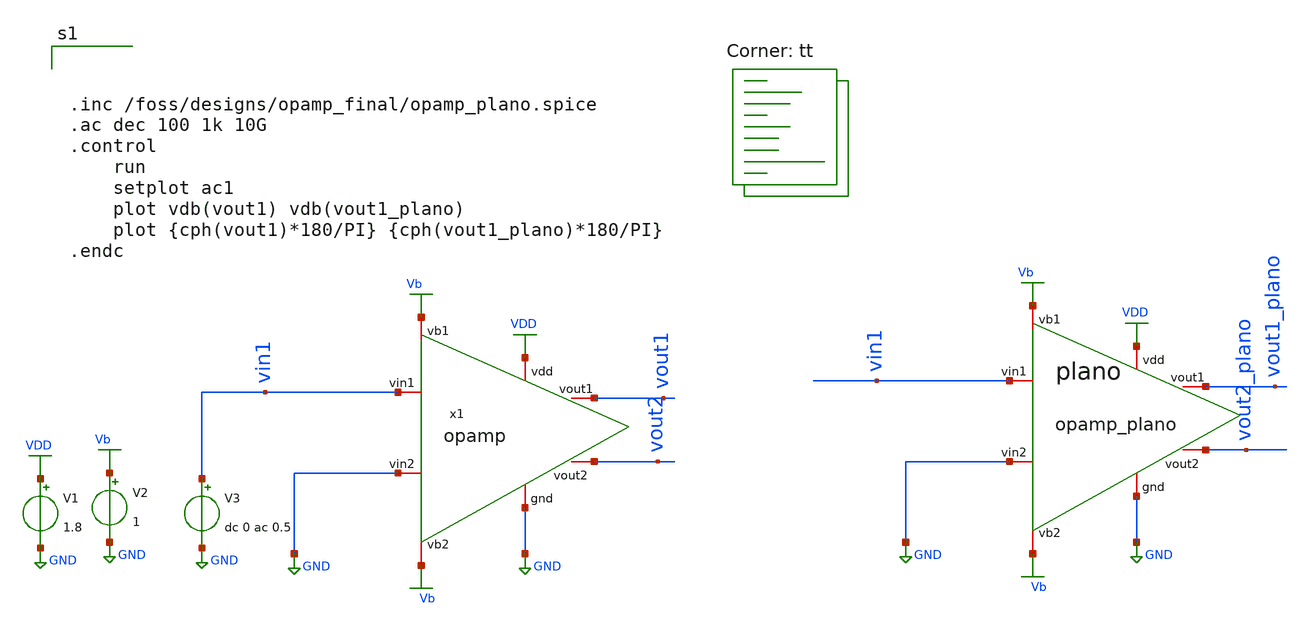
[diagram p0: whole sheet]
** sch_path: DIA3/opamp_final/tb_opamp_con_pex.sch
**.subckt tb_opamp_con_pex
x1 VDD Vb GND vin1 vout2 vout1 Vb GND opamp
V1 VDD GND 1.8
V3 vin1 GND dc 0 ac 0.5
V2 Vb GND 1
x1 VDD Vb GND vin1 vout2_plano vout1_plano GND Vb opamp_plano
**** begin user architecture code
.lib $::SKYWATER_MODELS/sky130.lib.spice tt



.inc /foss/designs/opamp_final/opamp_plano.spice
.ac dec 100 1k 10G
.control
	run
	setplot ac1
	plot vdb(vout1) vdb(vout1_plano)
	plot {cph(vout1)*180/PI} {cph(vout1_plano)*180/PI}
.endc



**** end user architecture code
**.ends

* expanding   symbol:  opamp.sym # of pins=8
** sym_path: DIA3/opamp_final/opamp.sym
** sch_path: DIA3/opamp_final/opamp.sch
.subckt opamp vdd vb1 vin2 vin1 vout2 vout1 vb2 gnd
*.iopin vdd
*.iopin gnd
*.iopin vout1
*.iopin vout2
*.iopin vin1
*.iopin vin2
*.iopin vb1
*.iopin vb2
XM1 X vb1 vdd vdd sky130_fd_pr__pfet_01v8 L=0.15 W=2.27 nf=1 ad='int((nf+1)/2) * W/nf * 0.29' as='int((nf+2)/2) * W/nf * 0.29'
+ pd='2*int((nf+1)/2) * (W/nf + 0.29)' ps='2*int((nf+2)/2) * (W/nf + 0.29)' nrd='0.29 / W' nrs='0.29 / W'
+ sa=0 sb=0 sd=0 mult=1 m=1
XM2 Y vb1 vdd vdd sky130_fd_pr__pfet_01v8 L=0.15 W=2.27 nf=1 ad='int((nf+1)/2) * W/nf * 0.29' as='int((nf+2)/2) * W/nf * 0.29'
+ pd='2*int((nf+1)/2) * (W/nf + 0.29)' ps='2*int((nf+2)/2) * (W/nf + 0.29)' nrd='0.29 / W' nrs='0.29 / W'
+ sa=0 sb=0 sd=0 mult=1 m=1
XM3 X vin2 net1 gnd sky130_fd_pr__nfet_01v8 L=0.15 W=0.86 nf=1 ad='int((nf+1)/2) * W/nf * 0.29' as='int((nf+2)/2) * W/nf * 0.29'
+ pd='2*int((nf+1)/2) * (W/nf + 0.29)' ps='2*int((nf+2)/2) * (W/nf + 0.29)' nrd='0.29 / W' nrs='0.29 / W'
+ sa=0 sb=0 sd=0 mult=1 m=1
XM4 Y vin1 net1 gnd sky130_fd_pr__nfet_01v8 L=0.15 W=0.86 nf=1 ad='int((nf+1)/2) * W/nf * 0.29' as='int((nf+2)/2) * W/nf * 0.29'
+ pd='2*int((nf+1)/2) * (W/nf + 0.29)' ps='2*int((nf+2)/2) * (W/nf + 0.29)' nrd='0.29 / W' nrs='0.29 / W'
+ sa=0 sb=0 sd=0 mult=1 m=1
XM5 net1 net2 gnd gnd sky130_fd_pr__nfet_01v8 L=0.15 W=0.49 nf=1 ad='int((nf+1)/2) * W/nf * 0.29' as='int((nf+2)/2) * W/nf * 0.29'
+ pd='2*int((nf+1)/2) * (W/nf + 0.29)' ps='2*int((nf+2)/2) * (W/nf + 0.29)' nrd='0.29 / W' nrs='0.29 / W'
+ sa=0 sb=0 sd=0 mult=1 m=1
XM6 vout1 Y vdd vdd sky130_fd_pr__pfet_01v8 L=0.15 W=56.9 nf=1 ad='int((nf+1)/2) * W/nf * 0.29' as='int((nf+2)/2) * W/nf * 0.29'
+ pd='2*int((nf+1)/2) * (W/nf + 0.29)' ps='2*int((nf+2)/2) * (W/nf + 0.29)' nrd='0.29 / W' nrs='0.29 / W'
+ sa=0 sb=0 sd=0 mult=1 m=1
XM7 vout2 X vdd vdd sky130_fd_pr__pfet_01v8 L=0.15 W=56.9 nf=1 ad='int((nf+1)/2) * W/nf * 0.29' as='int((nf+2)/2) * W/nf * 0.29'
+ pd='2*int((nf+1)/2) * (W/nf + 0.29)' ps='2*int((nf+2)/2) * (W/nf + 0.29)' nrd='0.29 / W' nrs='0.29 / W'
+ sa=0 sb=0 sd=0 mult=1 m=1
XM8 vout1 vb2 gnd gnd sky130_fd_pr__nfet_01v8 L=0.15 W=1.34 nf=1 ad='int((nf+1)/2) * W/nf * 0.29' as='int((nf+2)/2) * W/nf * 0.29'
+ pd='2*int((nf+1)/2) * (W/nf + 0.29)' ps='2*int((nf+2)/2) * (W/nf + 0.29)' nrd='0.29 / W' nrs='0.29 / W'
+ sa=0 sb=0 sd=0 mult=1 m=1
XM9 vout2 vb2 gnd gnd sky130_fd_pr__nfet_01v8 L=0.15 W=1.34 nf=1 ad='int((nf+1)/2) * W/nf * 0.29' as='int((nf+2)/2) * W/nf * 0.29'
+ pd='2*int((nf+1)/2) * (W/nf + 0.29)' ps='2*int((nf+2)/2) * (W/nf + 0.29)' nrd='0.29 / W' nrs='0.29 / W'
+ sa=0 sb=0 sd=0 mult=1 m=1
XM10 net2 net2 gnd gnd sky130_fd_pr__nfet_01v8 L=0.15 W=29 nf=1 ad='int((nf+1)/2) * W/nf * 0.29' as='int((nf+2)/2) * W/nf * 0.29'
+ pd='2*int((nf+1)/2) * (W/nf + 0.29)' ps='2*int((nf+2)/2) * (W/nf + 0.29)' nrd='0.29 / W' nrs='0.29 / W'
+ sa=0 sb=0 sd=0 mult=1 m=1
XR2 net2 vdd sky130_fd_pr__res_generic_po W=1 L=3.95 m=1
.ends

.GLOBAL VDD
.GLOBAL Vb
.GLOBAL GND
.end
